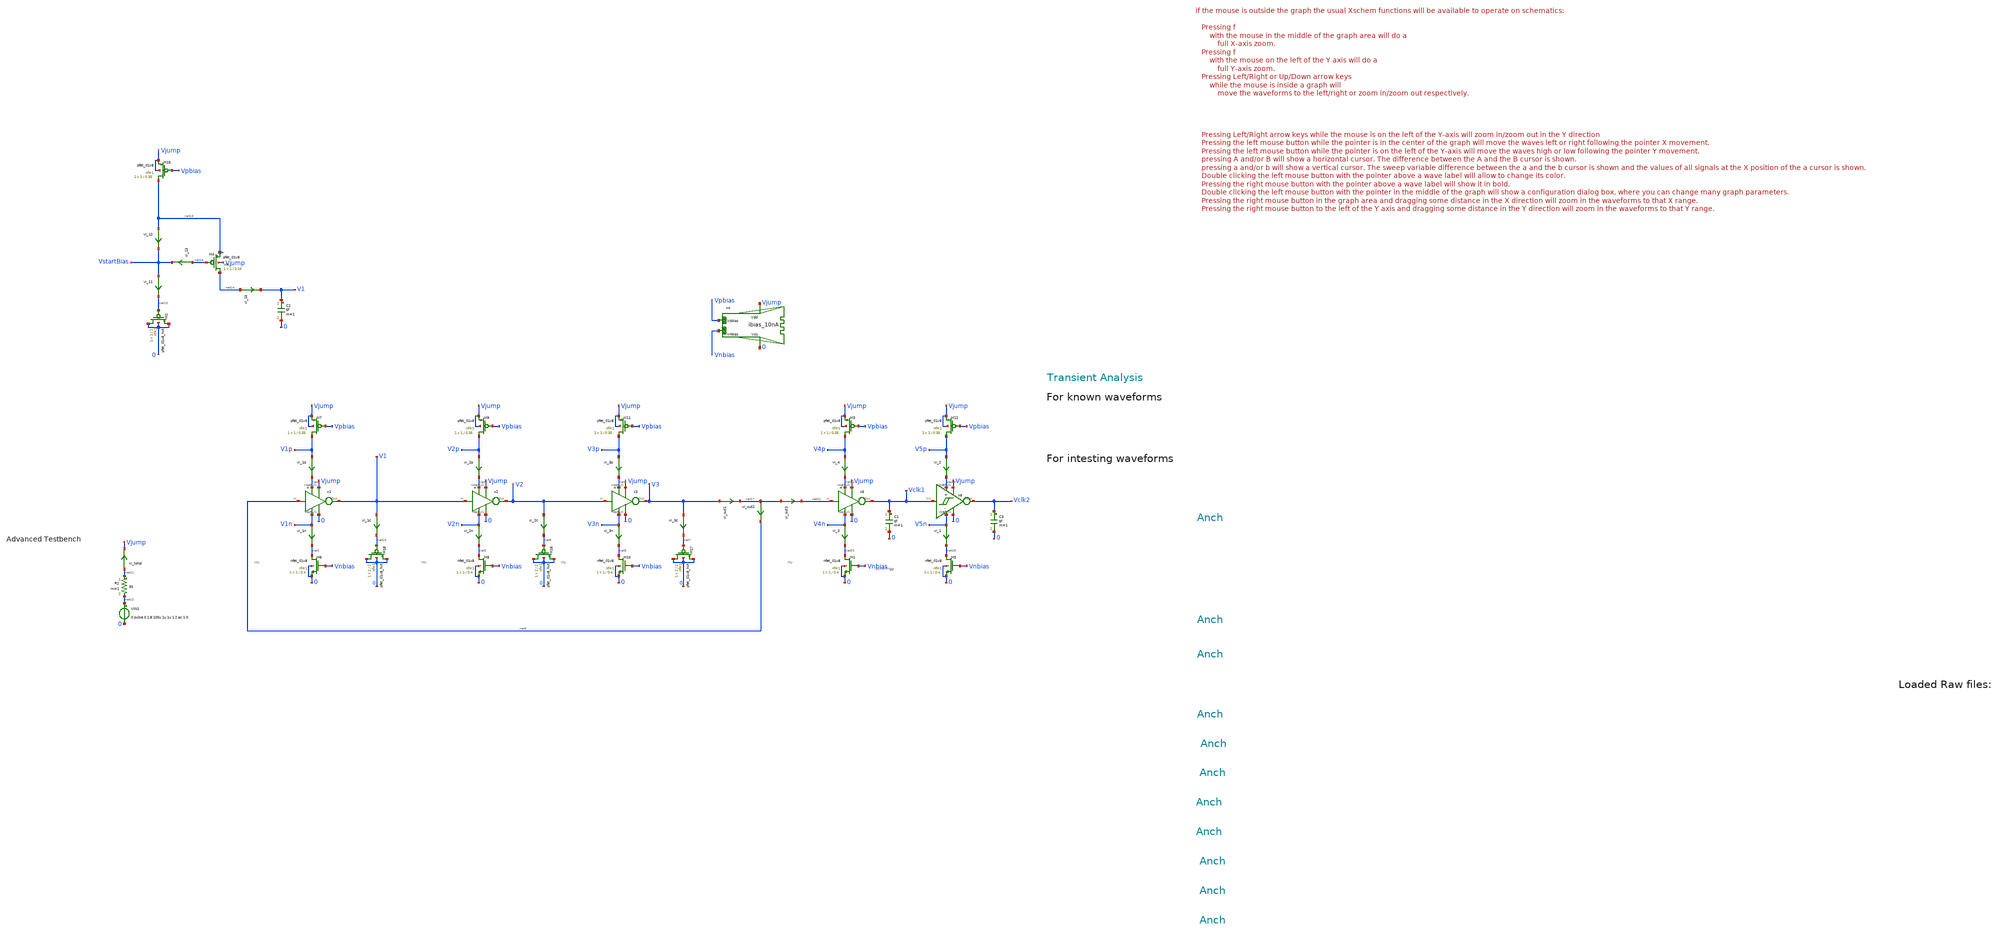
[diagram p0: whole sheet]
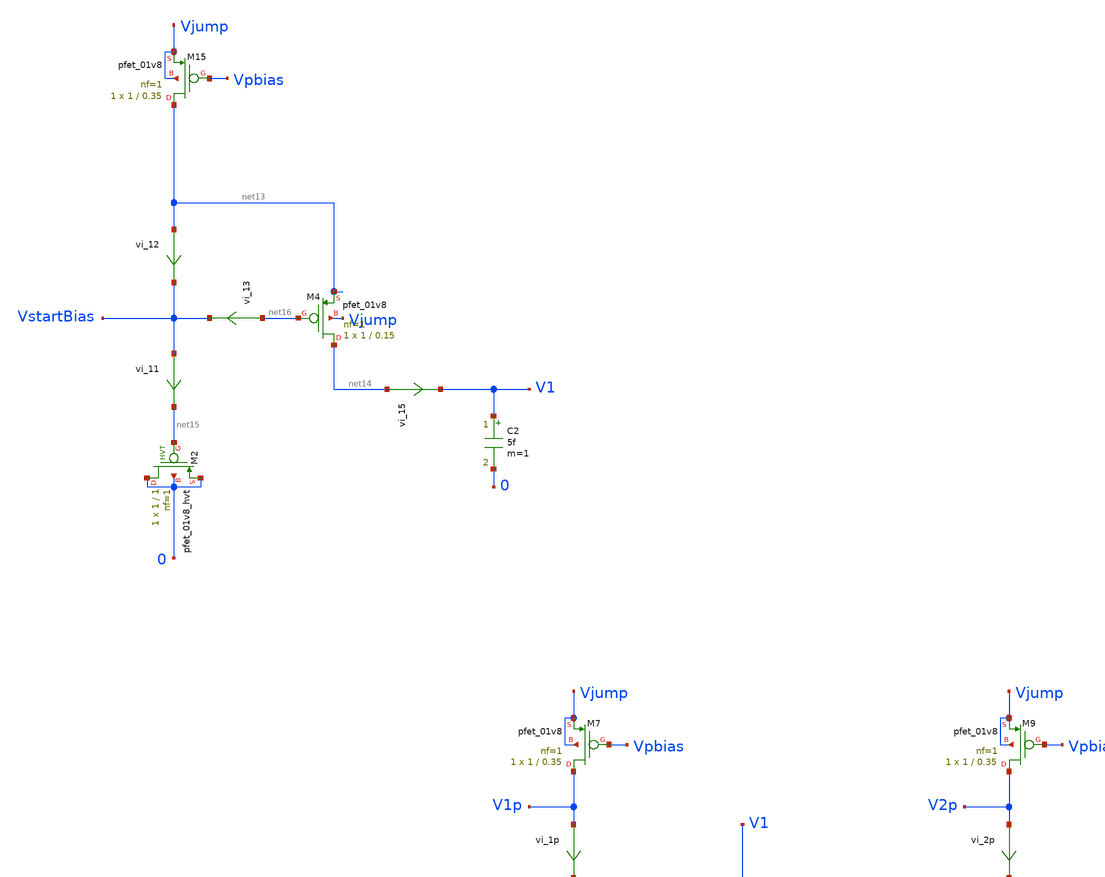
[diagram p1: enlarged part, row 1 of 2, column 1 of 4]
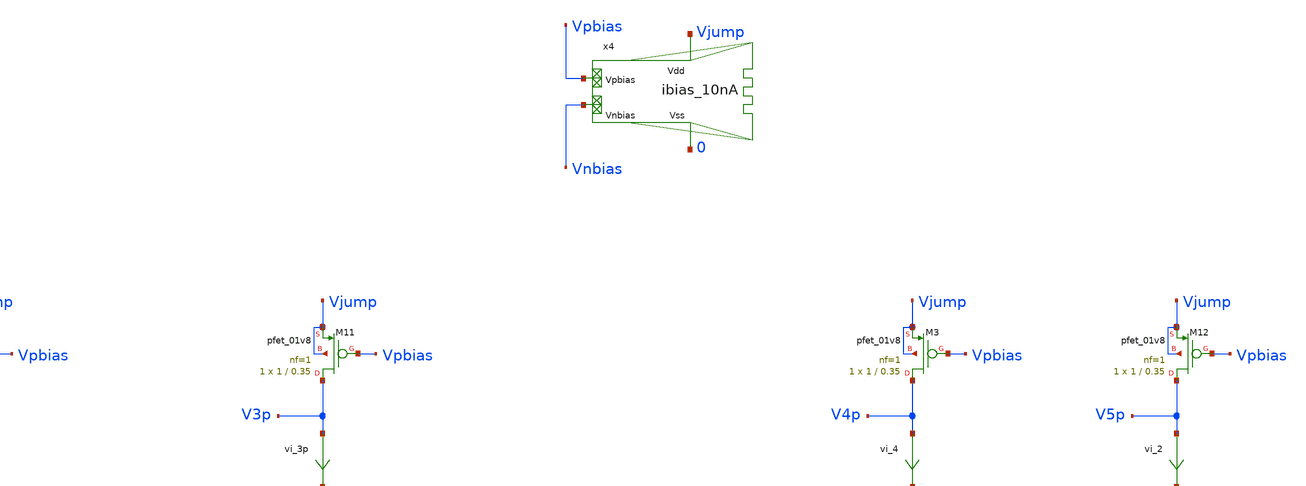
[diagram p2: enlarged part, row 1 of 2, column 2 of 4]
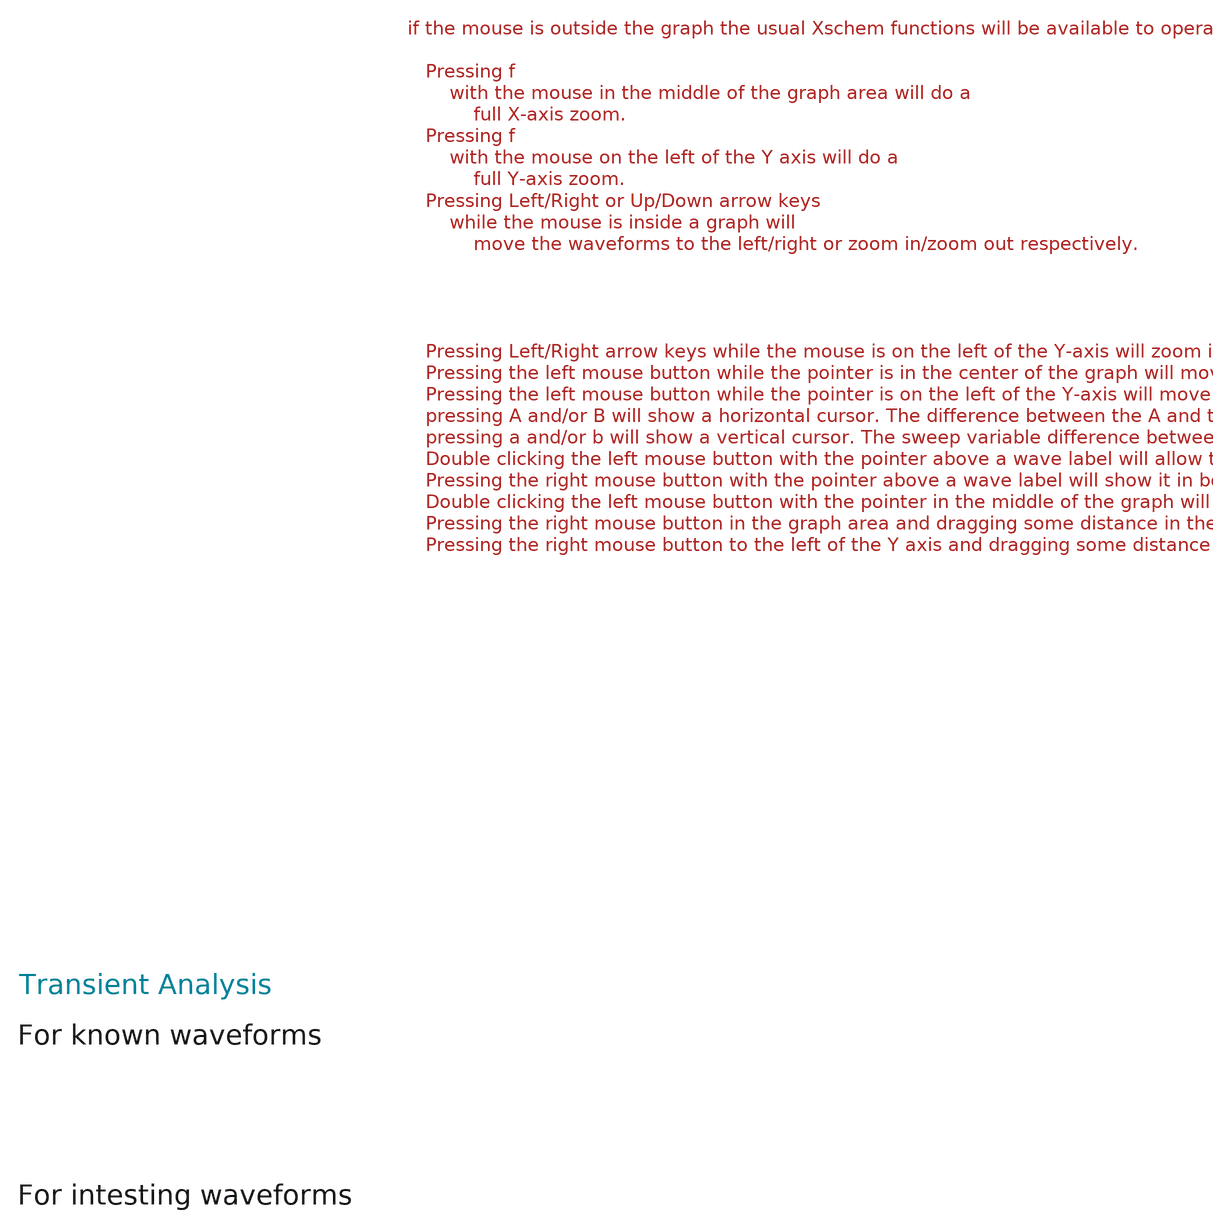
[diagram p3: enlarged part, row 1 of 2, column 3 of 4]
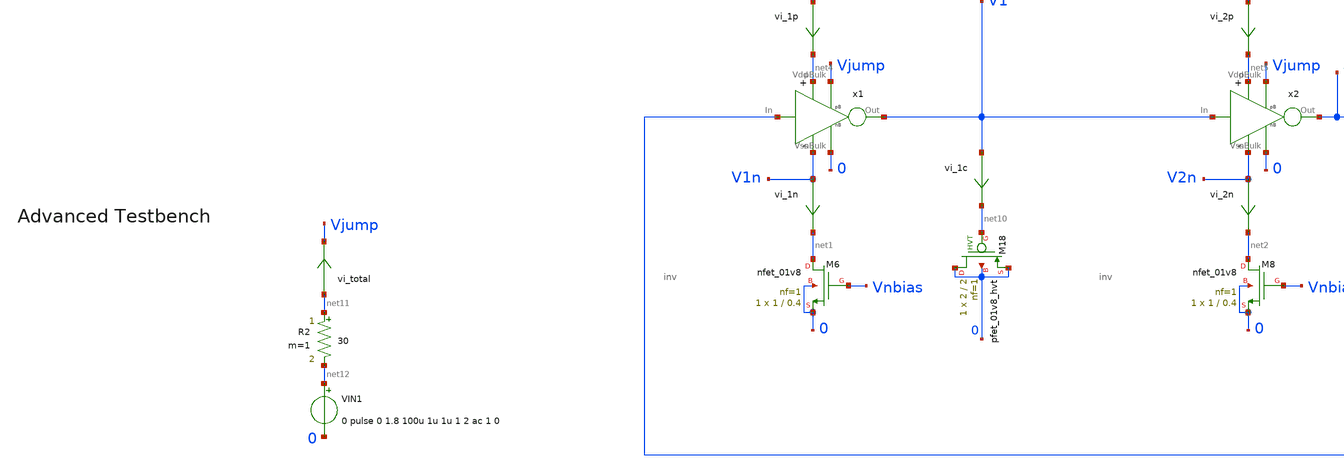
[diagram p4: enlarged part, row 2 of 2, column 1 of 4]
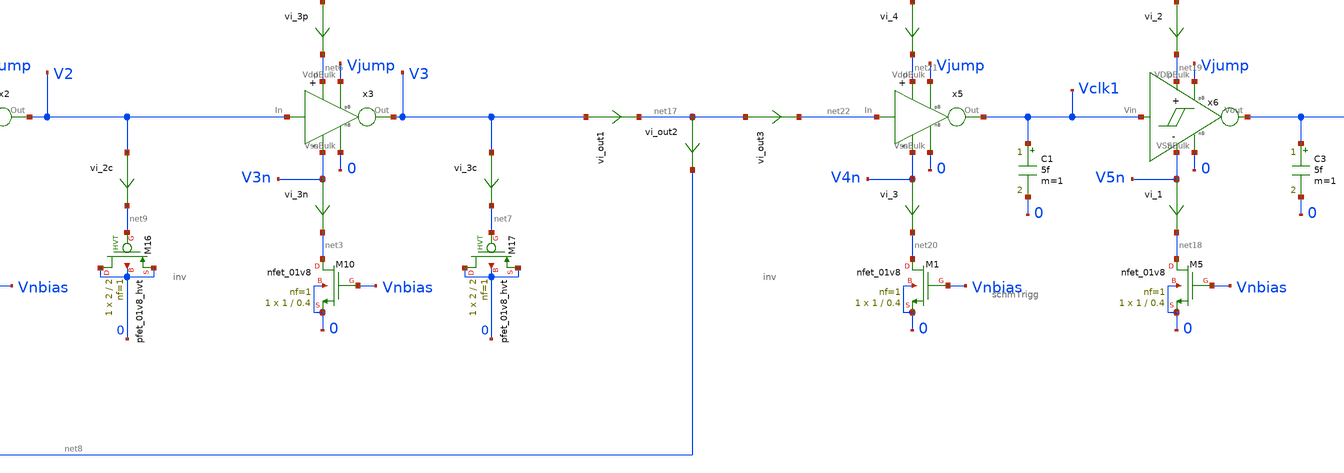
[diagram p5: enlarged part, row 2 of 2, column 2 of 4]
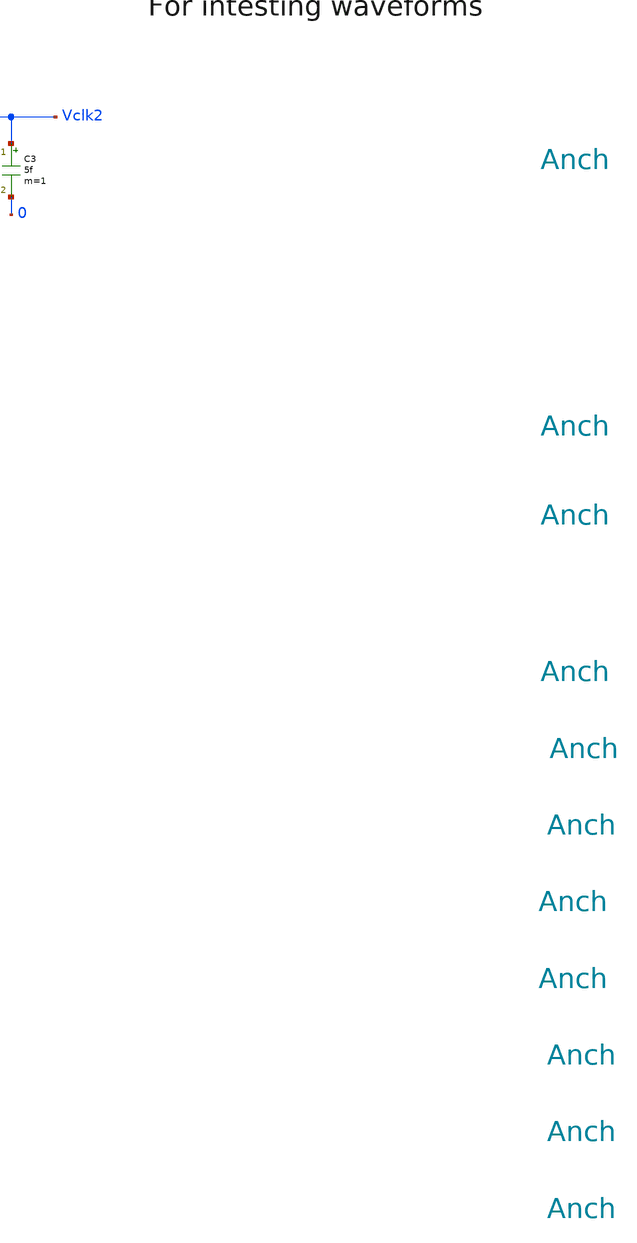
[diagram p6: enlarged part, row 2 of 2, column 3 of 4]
** sch_path: tt10-hdl/tt_um_test_commit/xschem/T3/oscillators/A_tt10_Ring_currentStarved/osc_tb.sch
* Copyright (C) 1998-2024 Stefan Frederik Schippers
* This program is free software; you can redistribute it and/or modify
* it under the terms of the GNU General Public License as published by
* the Free Software Foundation; either version 2 of the License, or
* (at your option) any later version.
* This program is distributed in the hope that it will be useful,
* but WITHOUT ANY WARRANTY; without even the implied warranty of
* MERCHANTABILITY or FITNESS FOR A PARTICULAR PURPOSE.  See the
* GNU General Public License for more details.
* You should have received a copy of the GNU General Public License
* along with this program; if not, write to the Free Software
**.subckt osc_tb
VIN1 net12 0 0 pulse 0 1.8 100u 1u 1u 1 2 ac 1 0
XM6 net1 Vnbias 0 0 sky130_fd_pr__nfet_01v8 L=0.4 W=1 nf=1 ad='int((1 + 1)/2) * 1 / 1 * 0.29' as='int((1 + 2)/2) * 1 / 1 * 0.29'
+ pd='2*int((1 + 1)/2) * (1 / 1 + 0.29)' ps='2*int((1 + 2)/2) * (1 / 1 + 0.29)' nrd='0.29 / 1 ' nrs='0.29 / 1 '
+ sa=0 sb=0 sd=0 mult=1 m=1
XM7 V1p Vpbias Vjump Vjump sky130_fd_pr__pfet_01v8 L=0.35 W=1 nf=1 ad='int((nf+1)/2) * W/nf * 0.29' as='int((nf+2)/2) * W/nf * 0.29'
+ pd='2*int((nf+1)/2) * (W/nf + 0.29)' ps='2*int((nf+2)/2) * (W/nf + 0.29)' nrd='0.29 / W' nrs='0.29 / W'
+ sa=0 sb=0 sd=0 mult=1 m=1
XM8 net2 Vnbias 0 0 sky130_fd_pr__nfet_01v8 L=0.4 W=1 nf=1 ad='int((1 + 1)/2) * 1 / 1 * 0.29' as='int((1 + 2)/2) * 1 / 1 * 0.29'
+ pd='2*int((1 + 1)/2) * (1 / 1 + 0.29)' ps='2*int((1 + 2)/2) * (1 / 1 + 0.29)' nrd='0.29 / 1 ' nrs='0.29 / 1 '
+ sa=0 sb=0 sd=0 mult=1 m=1
XM9 V2p Vpbias Vjump Vjump sky130_fd_pr__pfet_01v8 L=0.35 W=1 nf=1 ad='int((nf+1)/2) * W/nf * 0.29' as='int((nf+2)/2) * W/nf * 0.29'
+ pd='2*int((nf+1)/2) * (W/nf + 0.29)' ps='2*int((nf+2)/2) * (W/nf + 0.29)' nrd='0.29 / W' nrs='0.29 / W'
+ sa=0 sb=0 sd=0 mult=1 m=1
XM10 net3 Vnbias 0 0 sky130_fd_pr__nfet_01v8 L=0.4 W=1 nf=1 ad='int((1 + 1)/2) * 1 / 1 * 0.29' as='int((1 + 2)/2) * 1 / 1 * 0.29'
+ pd='2*int((1 + 1)/2) * (1 / 1 + 0.29)' ps='2*int((1 + 2)/2) * (1 / 1 + 0.29)' nrd='0.29 / 1 ' nrs='0.29 / 1 '
+ sa=0 sb=0 sd=0 mult=1 m=1
XM11 V3p Vpbias Vjump Vjump sky130_fd_pr__pfet_01v8 L=0.35 W=1 nf=1 ad='int((nf+1)/2) * W/nf * 0.29'
+ as='int((nf+2)/2) * W/nf * 0.29' pd='2*int((nf+1)/2) * (W/nf + 0.29)' ps='2*int((nf+2)/2) * (W/nf + 0.29)'
+ nrd='0.29 / W' nrs='0.29 / W' sa=0 sb=0 sd=0 mult=1 m=1
vi_1n V1n net1 0
.save i(vi_1n)
XM17 0 net7 0 0 sky130_fd_pr__pfet_01v8_hvt L=2 W=2 nf=1 ad='int((1 + 1)/2) * 2 / 1 * 0.29' as='int((1 + 2)/2) * 2 / 1 * 0.29'
+ pd='2*int((1 + 1)/2) * (2 / 1 + 0.29)' ps='2*int((1 + 2)/2) * (2 / 1 + 0.29)' nrd='0.29 / 2 ' nrs='0.29 / 2 '
+ sa=0 sb=0 sd=0 mult=1 m=1
vi_2n V2n net2 0
.save i(vi_2n)
vi_3n V3n net3 0
.save i(vi_3n)
vi_3c V3 net7 0
.save i(vi_3c)
vi_1p V1p net4 0
.save i(vi_1p)
vi_2p V2p net5 0
.save i(vi_2p)
vi_3p V3p net6 0
.save i(vi_3p)
XM16 0 net9 0 0 sky130_fd_pr__pfet_01v8_hvt L=2 W=2 nf=1 ad='int((1 + 1)/2) * 2 / 1 * 0.29' as='int((1 + 2)/2) * 2 / 1 * 0.29'
+ pd='2*int((1 + 1)/2) * (2 / 1 + 0.29)' ps='2*int((1 + 2)/2) * (2 / 1 + 0.29)' nrd='0.29 / 2 ' nrs='0.29 / 2 '
+ sa=0 sb=0 sd=0 mult=1 m=1
vi_2c V2 net9 0
.save i(vi_2c)
XM18 0 net10 0 0 sky130_fd_pr__pfet_01v8_hvt L=2 W=2 nf=1 ad='int((1 + 1)/2) * 2 / 1 * 0.29' as='int((1 + 2)/2) * 2 / 1 * 0.29'
+ pd='2*int((1 + 1)/2) * (2 / 1 + 0.29)' ps='2*int((1 + 2)/2) * (2 / 1 + 0.29)' nrd='0.29 / 2 ' nrs='0.29 / 2 '
+ sa=0 sb=0 sd=0 mult=1 m=1
vi_1c V1 net10 0
.save i(vi_1c)
vi_total net11 Vjump 0
.save i(vi_total)
R2 net11 net12 30 m=1
XM4 net14 net16 net13 Vjump sky130_fd_pr__pfet_01v8 L=0.15 W=1 nf=1 ad='int((nf+1)/2) * W/nf * 0.29'
+ as='int((nf+2)/2) * W/nf * 0.29' pd='2*int((nf+1)/2) * (W/nf + 0.29)' ps='2*int((nf+2)/2) * (W/nf + 0.29)'
+ nrd='0.29 / W' nrs='0.29 / W' sa=0 sb=0 sd=0 mult=1 m=1
XM2 0 net15 0 0 sky130_fd_pr__pfet_01v8_hvt L=1 W=1 nf=1 ad='int((1 + 1)/2) * 1 / 1 * 0.29' as='int((1 + 2)/2) * 1 / 1 * 0.29'
+ pd='2*int((1 + 1)/2) * (1 / 1 + 0.29)' ps='2*int((1 + 2)/2) * (1 / 1 + 0.29)' nrd='0.29 / 1 ' nrs='0.29 / 1 '
+ sa=0 sb=0 sd=0 mult=1 m=1
C2 V1 0 5f m=1
vi_11 VstartBias net15 0
.save i(vi_11)
vi_12 net13 VstartBias 0
.save i(vi_12)
XM15 net13 Vpbias Vjump Vjump sky130_fd_pr__pfet_01v8 L=0.35 W=1 nf=1 ad='int((nf+1)/2) * W/nf * 0.29'
+ as='int((nf+2)/2) * W/nf * 0.29' pd='2*int((nf+1)/2) * (W/nf + 0.29)' ps='2*int((nf+2)/2) * (W/nf + 0.29)'
+ nrd='0.29 / W' nrs='0.29 / W' sa=0 sb=0 sd=0 mult=1 m=1
vi_13 net16 VstartBias 0
.save i(vi_13)
vi_15 net14 V1 0
.save i(vi_15)
x1 net4 V1n V1 net8 0 Vjump inv
x2 net5 V2n V2 V1 0 Vjump inv
x3 net6 V3n V3 V2 0 Vjump inv
x4 Vjump 0 Vnbias Vpbias ibias_10nA
C1 Vclk1 0 5f m=1
vi_out1 V3 net17 0
.save i(vi_out1)
vi_out2 net17 net8 0
.save i(vi_out2)
vi_out3 net17 net22 0
.save i(vi_out3)
XM5 net18 Vnbias 0 0 sky130_fd_pr__nfet_01v8 L=0.4 W=1 nf=1 ad='int((1 + 1)/2) * 1 / 1 * 0.29' as='int((1 + 2)/2) * 1 / 1 * 0.29'
+ pd='2*int((1 + 1)/2) * (1 / 1 + 0.29)' ps='2*int((1 + 2)/2) * (1 / 1 + 0.29)' nrd='0.29 / 1 ' nrs='0.29 / 1 '
+ sa=0 sb=0 sd=0 mult=1 m=1
XM12 V5p Vpbias Vjump Vjump sky130_fd_pr__pfet_01v8 L=0.35 W=1 nf=1 ad='int((nf+1)/2) * W/nf * 0.29'
+ as='int((nf+2)/2) * W/nf * 0.29' pd='2*int((nf+1)/2) * (W/nf + 0.29)' ps='2*int((nf+2)/2) * (W/nf + 0.29)'
+ nrd='0.29 / W' nrs='0.29 / W' sa=0 sb=0 sd=0 mult=1 m=1
vi_1 V5n net18 0
.save i(vi_1)
vi_2 V5p net19 0
.save i(vi_2)
x6 Vclk1 V5n net19 Vclk2 Vjump 0 schmTrigg
C3 Vclk2 0 5f m=1
XM1 net20 Vnbias 0 0 sky130_fd_pr__nfet_01v8 L=0.4 W=1 nf=1 ad='int((1 + 1)/2) * 1 / 1 * 0.29' as='int((1 + 2)/2) * 1 / 1 * 0.29'
+ pd='2*int((1 + 1)/2) * (1 / 1 + 0.29)' ps='2*int((1 + 2)/2) * (1 / 1 + 0.29)' nrd='0.29 / 1 ' nrs='0.29 / 1 '
+ sa=0 sb=0 sd=0 mult=1 m=1
XM3 V4p Vpbias Vjump Vjump sky130_fd_pr__pfet_01v8 L=0.35 W=1 nf=1 ad='int((nf+1)/2) * W/nf * 0.29' as='int((nf+2)/2) * W/nf * 0.29'
+ pd='2*int((nf+1)/2) * (W/nf + 0.29)' ps='2*int((nf+2)/2) * (W/nf + 0.29)' nrd='0.29 / W' nrs='0.29 / W'
+ sa=0 sb=0 sd=0 mult=1 m=1
vi_3 V4n net20 0
.save i(vi_3)
vi_4 V4p net21 0
.save i(vi_4)
x5 net21 V4n Vclk1 net22 0 Vjump inv
**** begin user architecture code



.temp 30
.param Vdd = 1.8
.param imax = 100e-9


.option savecurrents
.save all
.control
  save all alli
  save

  op
  write template_adv_tb.raw
  set appendwrite


  tran 0.1u 1.1m
  write template_adv_tb.raw





  quit 0




.endc





** opencircuitdesign pdks install
.lib $::SKYWATER_MODELS/sky130.lib.spice tt


**** end user architecture code
**.ends

* expanding   symbol:  T0/inv/inv.sym # of pins=6
** sym_path: tt10-hdl/tt_um_test_commit/xschem/T0/inv/inv.sym
** sch_path: tt10-hdl/tt_um_test_commit/xschem/T0/inv/inv.sch
.subckt inv Vdd Vss Out In nBulk pBulk
*.ipin Vdd
*.ipin Vss
*.opin Out
*.ipin In
*.ipin nBulk
*.ipin pBulk
XM1 Out In Vss nBulk sky130_fd_pr__nfet_01v8 L=0.15 W=1 nf=1 ad='int((1 + 1)/2) * 1 / 1 * 0.29' as='int((1 + 2)/2) * 1 / 1 * 0.29'
+ pd='2*int((1 + 1)/2) * (1 / 1 + 0.29)' ps='2*int((1 + 2)/2) * (1 / 1 + 0.29)' nrd='0.29 / 1 ' nrs='0.29 / 1 '
+ sa=0 sb=0 sd=0 mult=1 m=1
XM2 Out In Vdd pBulk sky130_fd_pr__pfet_01v8 L=0.15 W=1 nf=1 ad='int((nf+1)/2) * W/nf * 0.29' as='int((nf+2)/2) * W/nf * 0.29'
+ pd='2*int((nf+1)/2) * (W/nf + 0.29)' ps='2*int((nf+2)/2) * (W/nf + 0.29)' nrd='0.29 / W' nrs='0.29 / W'
+ sa=0 sb=0 sd=0 mult=1 m=1
.ends


* expanding   symbol:  T2/biasGen/A_tt10_10nA/ibias_10nA.sym # of pins=4
** sym_path: tt10-hdl/tt_um_test_commit/xschem/T2/biasGen/A_tt10_10nA/ibias_10nA.sym
** sch_path: tt10-hdl/tt_um_test_commit/xschem/T2/biasGen/A_tt10_10nA/ibias_10nA.sch
.subckt ibias_10nA Vdd Vss Vnbias Vpbias
*.ipin Vdd
*.ipin Vss
*.opin Vnbias
*.opin Vpbias
XM3 Vpbias Vpbias Vdd Vdd sky130_fd_pr__pfet_01v8 L=0.35 W=0.5 nf=1 ad='int((nf+1)/2) * W/nf * 0.29'
+ as='int((nf+2)/2) * W/nf * 0.29' pd='2*int((nf+1)/2) * (W/nf + 0.29)' ps='2*int((nf+2)/2) * (W/nf + 0.29)'
+ nrd='0.29 / W' nrs='0.29 / W' sa=0 sb=0 sd=0 mult=1 m=1
XM4 Vnbias Vpbias Vdd Vdd sky130_fd_pr__pfet_01v8 L=0.35 W=0.5 nf=1 ad='int((nf+1)/2) * W/nf * 0.29'
+ as='int((nf+2)/2) * W/nf * 0.29' pd='2*int((nf+1)/2) * (W/nf + 0.29)' ps='2*int((nf+2)/2) * (W/nf + 0.29)'
+ nrd='0.29 / W' nrs='0.29 / W' sa=0 sb=0 sd=0 mult=1 m=1
XM5 net2 Vpbias Vdd Vdd sky130_fd_pr__pfet_01v8 L=0.35 W=1 nf=1 ad='int((nf+1)/2) * W/nf * 0.29' as='int((nf+2)/2) * W/nf * 0.29'
+ pd='2*int((nf+1)/2) * (W/nf + 0.29)' ps='2*int((nf+2)/2) * (W/nf + 0.29)' nrd='0.29 / W' nrs='0.29 / W'
+ sa=0 sb=0 sd=0 mult=1 m=1
XM1 Vpbias Vnbias net1 Vss sky130_fd_pr__nfet_01v8 L=0.2 W=0.5 nf=1 ad='int((1 + 1)/2) * 0.5 / 1 * 0.29'
+ as='int((1 + 2)/2) * 0.5 / 1 * 0.29' pd='2*int((1 + 1)/2) * (0.5 / 1 + 0.29)' ps='2*int((1 + 2)/2) * (0.5 / 1 + 0.29)'
+ nrd='0.29 / 0.5 ' nrs='0.29 / 0.5 ' sa=0 sb=0 sd=0 mult=1 m=1
XM2 Vnbias Vnbias Vss Vss sky130_fd_pr__nfet_01v8 L=0.2 W=0.5 nf=1 ad='int((1 + 1)/2) * 0.5 / 1 * 0.29'
+ as='int((1 + 2)/2) * 0.5 / 1 * 0.29' pd='2*int((1 + 1)/2) * (0.5 / 1 + 0.29)' ps='2*int((1 + 2)/2) * (0.5 / 1 + 0.29)'
+ nrd='0.29 / 0.5 ' nrs='0.29 / 0.5 ' sa=0 sb=0 sd=0 mult=1 m=1
XM6 net2 net2 net1 Vss sky130_fd_pr__nfet_01v8 L=0.2 W=1 nf=1 ad='int((1 + 1)/2) * 1 / 1 * 0.29' as='int((1 + 2)/2) * 1 / 1 * 0.29'
+ pd='2*int((1 + 1)/2) * (1 / 1 + 0.29)' ps='2*int((1 + 2)/2) * (1 / 1 + 0.29)' nrd='0.29 / 1 ' nrs='0.29 / 1 '
+ sa=0 sb=0 sd=0 mult=1 m=1
XM7 net1 net2 Vss Vss sky130_fd_pr__nfet_01v8 L=1 W=1 nf=1 ad='int((1 + 1)/2) * 1 / 1 * 0.29' as='int((1 + 2)/2) * 1 / 1 * 0.29'
+ pd='2*int((1 + 1)/2) * (1 / 1 + 0.29)' ps='2*int((1 + 2)/2) * (1 / 1 + 0.29)' nrd='0.29 / 1 ' nrs='0.29 / 1 '
+ sa=0 sb=0 sd=0 mult=1 m=1
.ends


* expanding   symbol:  T1/schmTrigg/schmTrigg.sym # of pins=6
** sym_path: tt10-hdl/tt_um_test_commit/xschem/T1/schmTrigg/schmTrigg.sym
** sch_path: tt10-hdl/tt_um_test_commit/xschem/T1/schmTrigg/schmTrigg.sch
.subckt schmTrigg Vin VSS VDD Vout pBulk nBulk
*.ipin Vin
*.ipin VDD
*.ipin VSS
*.opin Vout
*.ipin nBulk
*.ipin pBulk
XM1 VDD Vout Vn nBulk sky130_fd_pr__nfet_01v8 L=0.15 W=1 nf=1 ad='int((1 + 1)/2) * 1 / 1 * 0.29' as='int((1 + 2)/2) * 1 / 1 * 0.29'
+ pd='2*int((1 + 1)/2) * (1 / 1 + 0.29)' ps='2*int((1 + 2)/2) * (1 / 1 + 0.29)' nrd='0.29 / 1 ' nrs='0.29 / 1 '
+ sa=0 sb=0 sd=0 mult=1 m=1
XM2 Vn Vin VSS nBulk sky130_fd_pr__nfet_01v8 L=0.15 W=1 nf=1 ad='int((1 + 1)/2) * 1 / 1 * 0.29' as='int((1 + 2)/2) * 1 / 1 * 0.29'
+ pd='2*int((1 + 1)/2) * (1 / 1 + 0.29)' ps='2*int((1 + 2)/2) * (1 / 1 + 0.29)' nrd='0.29 / 1 ' nrs='0.29 / 1 '
+ sa=0 sb=0 sd=0 mult=1 m=1
XM3 Vout Vin Vn nBulk sky130_fd_pr__nfet_01v8 L=0.15 W=1 nf=1 ad='int((1 + 1)/2) * 1 / 1 * 0.29' as='int((1 + 2)/2) * 1 / 1 * 0.29'
+ pd='2*int((1 + 1)/2) * (1 / 1 + 0.29)' ps='2*int((1 + 2)/2) * (1 / 1 + 0.29)' nrd='0.29 / 1 ' nrs='0.29 / 1 '
+ sa=0 sb=0 sd=0 mult=1 m=1
XM4 VSS Vout Vp pBulk sky130_fd_pr__pfet_01v8 L=0.15 W=1 nf=1 ad='int((nf+1)/2) * W/nf * 0.29' as='int((nf+2)/2) * W/nf * 0.29'
+ pd='2*int((nf+1)/2) * (W/nf + 0.29)' ps='2*int((nf+2)/2) * (W/nf + 0.29)' nrd='0.29 / W' nrs='0.29 / W'
+ sa=0 sb=0 sd=0 mult=1 m=1
XM5 Vout Vin Vp pBulk sky130_fd_pr__pfet_01v8 L=0.15 W=1 nf=1 ad='int((nf+1)/2) * W/nf * 0.29' as='int((nf+2)/2) * W/nf * 0.29'
+ pd='2*int((nf+1)/2) * (W/nf + 0.29)' ps='2*int((nf+2)/2) * (W/nf + 0.29)' nrd='0.29 / W' nrs='0.29 / W'
+ sa=0 sb=0 sd=0 mult=1 m=1
XM6 Vp Vin VDD pBulk sky130_fd_pr__pfet_01v8 L=0.15 W=1 nf=1 ad='int((nf+1)/2) * W/nf * 0.29' as='int((nf+2)/2) * W/nf * 0.29'
+ pd='2*int((nf+1)/2) * (W/nf + 0.29)' ps='2*int((nf+2)/2) * (W/nf + 0.29)' nrd='0.29 / W' nrs='0.29 / W'
+ sa=0 sb=0 sd=0 mult=1 m=1
.ends

.end
